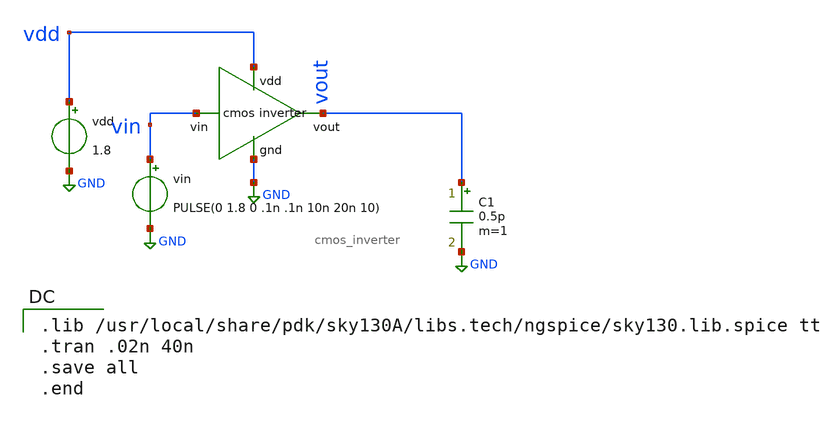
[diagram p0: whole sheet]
** sch_path: schematic/cmos_inverter_test.sch
**.subckt cmos_inverter_test
x1 vdd vin vout GND cmos_inverter
vdd vdd GND 1.8
vin vin GND PULSE(0 1.8 0 .1n .1n 10n 20n 10)
C1 vout GND 0.5p m=1
**** begin user architecture code

.lib /usr/local/share/pdk/sky130A/libs.tech/ngspice/sky130.lib.spice tt
.tran .02n 40n
.save all
.end

**** end user architecture code
**.ends

* expanding   symbol:  cmos_inverter.sym # of pins=4
** sym_path: schematic/cmos_inverter.sym
** sch_path: schematic/cmos_inverter.sch
.subckt cmos_inverter vdd vin vout gnd
*.ipin vin
*.ipin vdd
*.ipin gnd
*.opin vout
XM1 vout vin gnd gnd sky130_fd_pr__nfet_01v8 L=0.15 W=1 nf=1 ad='int((1 + 1)/2) * 1 / 1 * 0.29' as='int((1 + 2)/2) * 1 / 1 * 0.29'
+ pd='2*int((1 + 1)/2) * (1 / 1 + 0.29)' ps='2*int((1 + 2)/2) * (1 / 1 + 0.29)' nrd='0.29 / 1 ' nrs='0.29 / 1 '
+ sa=0 sb=0 sd=0 mult=1 m=1
XM2 vout vin vdd vdd sky130_fd_pr__pfet_01v8 L=0.15 W=2.5 nf=1 ad='int((1 + 1)/2) * 2.5 / 1 * 0.29' as='int((1 + 2)/2) * 2.5 / 1 * 0.29'
+ pd='2*int((1 + 1)/2) * (2.5 / 1 + 0.29)' ps='2*int((1 + 2)/2) * (2.5 / 1 + 0.29)' nrd='0.29 / 2.5 ' nrs='0.29 / 2.5 '
+ sa=0 sb=0 sd=0 mult=1 m=1
.ends

.GLOBAL GND
.end
